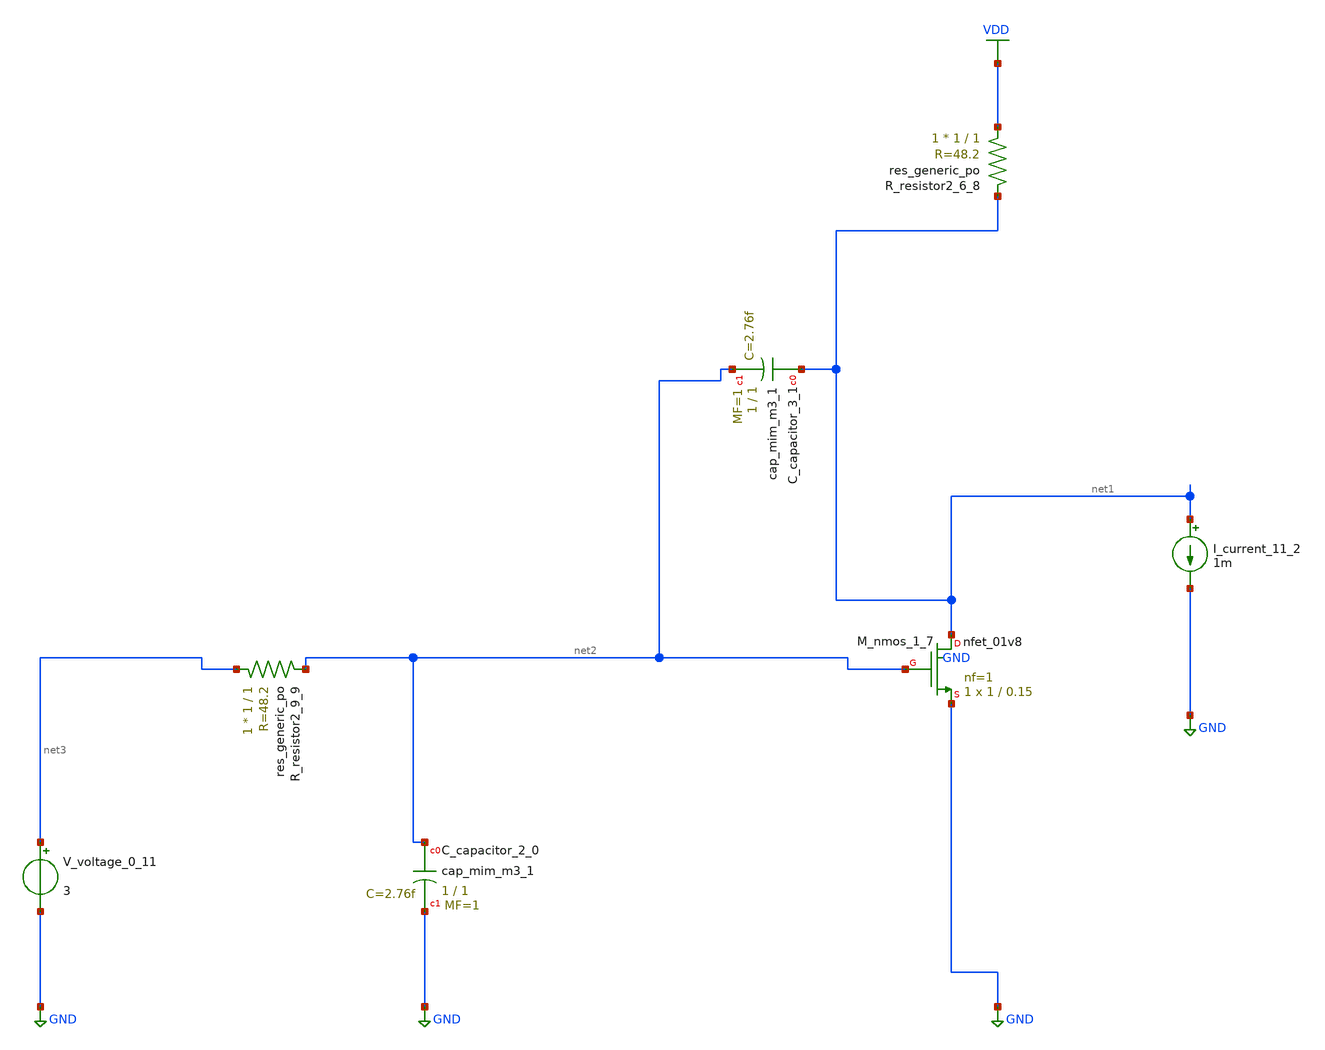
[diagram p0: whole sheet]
** sch_path: schematics/AMSNet/365.sch
**.subckt 365
XC_capacitor_2_0 net2 GND sky130_fd_pr__cap_mim_m3_1 W=1 L=1 MF=1 m=1
XC_capacitor_3_1 net1 net2 sky130_fd_pr__cap_mim_m3_1 W=1 L=1 MF=1 m=1
I_current_11_2 net1 GND 1m
XM_nmos_1_7 net1 net2 GND GND sky130_fd_pr__nfet_01v8 L=0.15 W=1 nf=1 ad='int((1 + 1)/2) * 1 / 1 * 0.29'
+ as='int((1 + 2)/2) * 1 / 1 * 0.29' pd='2*int((1 + 1)/2) * (1 / 1 + 0.29)' ps='2*int((1 + 2)/2) * (1 / 1 + 0.29)'
+ nrd='0.29 / 1 ' nrs='0.29 / 1 ' sa=0 sb=0 sd=0 mult=1 m=1
XR_resistor2_6_8 VDD net1 sky130_fd_pr__res_generic_po W=1 L=1 m=1
XR_resistor2_9_9 net3 net2 sky130_fd_pr__res_generic_po W=1 L=1 m=1
V_voltage_0_11 net3 GND 3
**.ends
.GLOBAL GND
.GLOBAL VDD
.end
